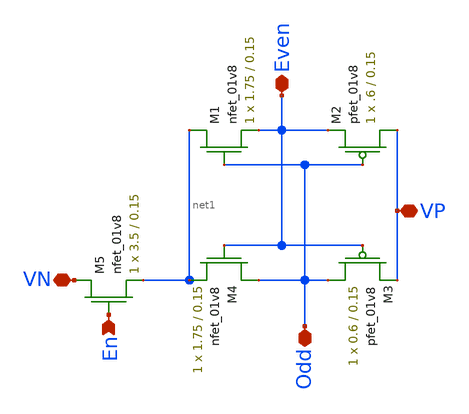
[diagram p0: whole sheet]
** sch_path: DRAM_Components/Schematic/SenseAmp.sch
**.subckt SenseAmp Odd En VN VP Even
*.iopin Odd
*.ipin En
*.iopin VN
*.iopin VP
*.iopin Even
XM1 net1 Odd Even GND sky130_fd_pr__nfet_01v8 L=0.15 W=1.75 nf=1 ad='int((nf+1)/2) * W/nf * 0.29' as='int((nf+2)/2) * W/nf * 0.29'
+ pd='2*int((nf+1)/2) * (W/nf + 0.29)' ps='2*int((nf+2)/2) * (W/nf + 0.29)' nrd='0.29 / W' nrs='0.29 / W'
+ sa=0 sb=0 sd=0 mult=1 m=1
XM2 VP Odd Even VDD sky130_fd_pr__pfet_01v8 L=0.15 W=.6 nf=1 ad='int((nf+1)/2) * W/nf * 0.29' as='int((nf+2)/2) * W/nf * 0.29'
+ pd='2*int((nf+1)/2) * (W/nf + 0.29)' ps='2*int((nf+2)/2) * (W/nf + 0.29)' nrd='0.29 / W' nrs='0.29 / W'
+ sa=0 sb=0 sd=0 mult=1 m=1
XM3 Odd Even VP VDD sky130_fd_pr__pfet_01v8 L=0.15 W=0.6 nf=1 ad='int((nf+1)/2) * W/nf * 0.29' as='int((nf+2)/2) * W/nf * 0.29'
+ pd='2*int((nf+1)/2) * (W/nf + 0.29)' ps='2*int((nf+2)/2) * (W/nf + 0.29)' nrd='0.29 / W' nrs='0.29 / W'
+ sa=0 sb=0 sd=0 mult=1 m=1
XM4 Odd Even net1 GND sky130_fd_pr__nfet_01v8 L=0.15 W=1.75 nf=1 ad='int((nf+1)/2) * W/nf * 0.29' as='int((nf+2)/2) * W/nf * 0.29'
+ pd='2*int((nf+1)/2) * (W/nf + 0.29)' ps='2*int((nf+2)/2) * (W/nf + 0.29)' nrd='0.29 / W' nrs='0.29 / W'
+ sa=0 sb=0 sd=0 mult=1 m=1
XM5 VN En net1 GND sky130_fd_pr__nfet_01v8 L=0.15 W=3.5 nf=1 ad='int((nf+1)/2) * W/nf * 0.29' as='int((nf+2)/2) * W/nf * 0.29'
+ pd='2*int((nf+1)/2) * (W/nf + 0.29)' ps='2*int((nf+2)/2) * (W/nf + 0.29)' nrd='0.29 / W' nrs='0.29 / W'
+ sa=0 sb=0 sd=0 mult=1 m=1
**.ends
.end
